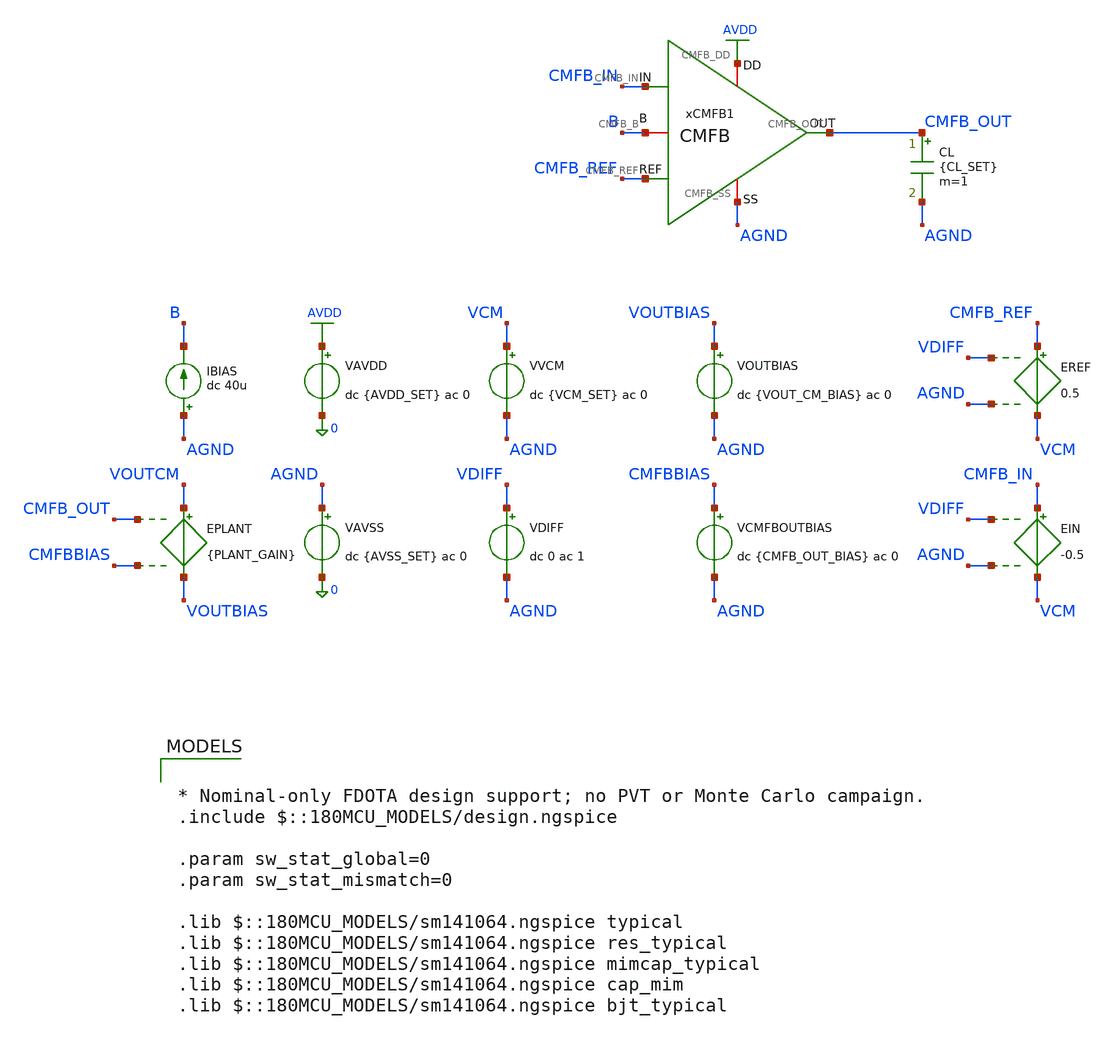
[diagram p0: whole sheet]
** sch_path: Design_Files/IC Design/Testbench/ANALOG_BLOCKS/FDOTA/CMFB/CMFB_TB_OL.sch
**.subckt CMFB_TB_OL
IBIAS AGND B dc 40u
VAVDD AVDD 0 dc {AVDD_SET} ac 0
.save i(vavdd)
CL CMFB_OUT AGND {CL_SET} m=1
VVCM VCM AGND dc {VCM_SET} ac 0
VDIFF VDIFF AGND dc 0 ac 1
VAVSS AGND 0 dc {AVSS_SET} ac 0
.save i(vavss)
VOUTBIAS VOUTBIAS AGND dc {VOUT_CM_BIAS} ac 0
VCMFBOUTBIAS CMFBBIAS AGND dc {CMFB_OUT_BIAS} ac 0
EREF CMFB_REF VCM VDIFF AGND 0.5
EIN CMFB_IN VCM VDIFF AGND -0.5
EPLANT VOUTCM VOUTBIAS CMFB_OUT CMFBBIAS {PLANT_GAIN}
xCMFB1 AVDD AGND CMFB_IN CMFB_REF CMFB_OUT B CMFB
**** begin user architecture code

* Nominal-only FDOTA design support; no PVT or Monte Carlo campaign.
.include $::180MCU_MODELS/design.ngspice

.param sw_stat_global=0
.param sw_stat_mismatch=0

.lib $::180MCU_MODELS/sm141064.ngspice typical
.lib $::180MCU_MODELS/sm141064.ngspice res_typical
.lib $::180MCU_MODELS/sm141064.ngspice mimcap_typical
.lib $::180MCU_MODELS/sm141064.ngspice cap_mim
.lib $::180MCU_MODELS/sm141064.ngspice bjt_typical




.control
destroy all
save all
set noaskquit
set wr_vecnames
set wr_singlescale
option numdgt=15

shell mkdir -p
+ /foss/designs/ECG_Acquisition_IC/Measurement_Results/IC_Simulation/ANALOG_BLOCKS/FDOTA/CMFB/Result_txt

shell rm -f
+ /foss/designs/ECG_Acquisition_IC/Measurement_Results/IC_Simulation/ANALOG_BLOCKS/FDOTA/CMFB/Result_txt/ol_ac.txt

let avdd_run = 3.3
let vcm_run  = avdd_run/2

alter @VAVDD[DC] = $&avdd_run
alter @VVCM[DC]  = $&vcm_run
alter @VDIFF[DC] = 0

alter @VVCM[ACMAG]   = 0
alter @VDIFF[ACMAG]  = 1
alter @VDIFF[ACPHASE] = 0
alter @VAVDD[ACMAG]  = 0
alter @VAVSS[ACMAG]  = 0

* Open-loop AC
ac dec 200 1 100G

let error_ac = v(cmfb_ref)-v(cmfb_in)
let loop_ac  = v(voutcm)/error_ac

let loop_real = real(loop_ac)
let loop_imag = imag(loop_ac)

setscale frequency

wrdata
+ /foss/designs/ECG_Acquisition_IC/Measurement_Results/IC_Simulation/ANALOG_BLOCKS/FDOTA/CMFB/Result_txt/ol_ac.txt loop_real loop_imag

quit
.endc




.param AVDD_SET=3.3
.param AVSS_SET=0
.param TEMP_SET=27
.param CL_SET=10p

.param VCM_SET={AVDD_SET/2}
.param VOUT_CM_BIAS={AVDD_SET/2}
.param CMFB_OUT_BIAS=2.4832

.param PLANT_GAIN=500

.temp {TEMP_SET}

.options gmin=1e-12 rshunt=1e12 method=gear
.nodeset v(B)=2.3 v(CMFB_OUT)={CMFB_OUT_BIAS} v(VOUTCM)={VOUT_CM_BIAS}


**** end user architecture code
**.ends

* expanding   symbol:  ECG_Acquisition_IC/Design_Files/IC
*+ Design/Schematic/ANALOG_BLOCKS/FDOTA/CMFB/CMFB.sym # of pins=6
** sym_path: Design_Files/IC Design/Schematic/FD_OTA/CMFB/CMFB.sym
** sch_path: Design_Files/IC Design/Schematic/FD_OTA/CMFB/CMFB.sch
.subckt CMFB CMFB_DD CMFB_SS CMFB_IN CMFB_REF CMFB_OUT CMFB_B
*.iopin CMFB_DD
*.iopin CMFB_SS
*.ipin CMFB_IN
*.ipin CMFB_REF
*.opin CMFB_OUT
*.iopin CMFB_B
XM4 CMFB_OUT CMFB_OUT CMFB_DD CMFB_DD pfet_03v3 L=0.5u W=1u nf=1 ad='int((nf+1)/2) * W/nf * 0.18u' as='int((nf+2)/2) * W/nf * 0.18u'
+ pd='2*int((nf+1)/2) * (W/nf + 0.18u)' ps='2*int((nf+2)/2) * (W/nf + 0.18u)' nrd='0.18u / W' nrs='0.18u / W'
+ sa=0 sb=0 sd=0 m=77
XM3 net2 net2 CMFB_DD CMFB_DD pfet_03v3 L=0.5u W=1u nf=1 ad='int((nf+1)/2) * W/nf * 0.18u' as='int((nf+2)/2) * W/nf * 0.18u'
+ pd='2*int((nf+1)/2) * (W/nf + 0.18u)' ps='2*int((nf+2)/2) * (W/nf + 0.18u)' nrd='0.18u / W' nrs='0.18u / W'
+ sa=0 sb=0 sd=0 m=77
XM1 net2 CMFB_REF net1 CMFB_SS nfet_03v3 L=0.5u W=1u nf=1 ad='int((nf+1)/2) * W/nf * 0.18u' as='int((nf+2)/2) * W/nf * 0.18u'
+ pd='2*int((nf+1)/2) * (W/nf + 0.18u)' ps='2*int((nf+2)/2) * (W/nf + 0.18u)' nrd='0.18u / W' nrs='0.18u / W'
+ sa=0 sb=0 sd=0 m=5
XM2 CMFB_OUT CMFB_IN net1 CMFB_SS nfet_03v3 L=0.5u W=1u nf=1 ad='int((nf+1)/2) * W/nf * 0.18u' as='int((nf+2)/2) * W/nf * 0.18u'
+ pd='2*int((nf+1)/2) * (W/nf + 0.18u)' ps='2*int((nf+2)/2) * (W/nf + 0.18u)' nrd='0.18u / W' nrs='0.18u / W'
+ sa=0 sb=0 sd=0 m=5
XM5 net1 CMFB_B CMFB_SS CMFB_SS nfet_03v3 L=2u W=1u nf=1 ad='int((nf+1)/2) * W/nf * 0.18u' as='int((nf+2)/2) * W/nf * 0.18u'
+ pd='2*int((nf+1)/2) * (W/nf + 0.18u)' ps='2*int((nf+2)/2) * (W/nf + 0.18u)' nrd='0.18u / W' nrs='0.18u / W'
+ sa=0 sb=0 sd=0 m=20
XM10 CMFB_B CMFB_B CMFB_SS CMFB_SS nfet_03v3 L=2u W=1u nf=1 ad='int((nf+1)/2) * W/nf * 0.18u' as='int((nf+2)/2) * W/nf * 0.18u'
+ pd='2*int((nf+1)/2) * (W/nf + 0.18u)' ps='2*int((nf+2)/2) * (W/nf + 0.18u)' nrd='0.18u / W' nrs='0.18u / W'
+ sa=0 sb=0 sd=0 m=20
.ends

.GLOBAL AVDD
.end
